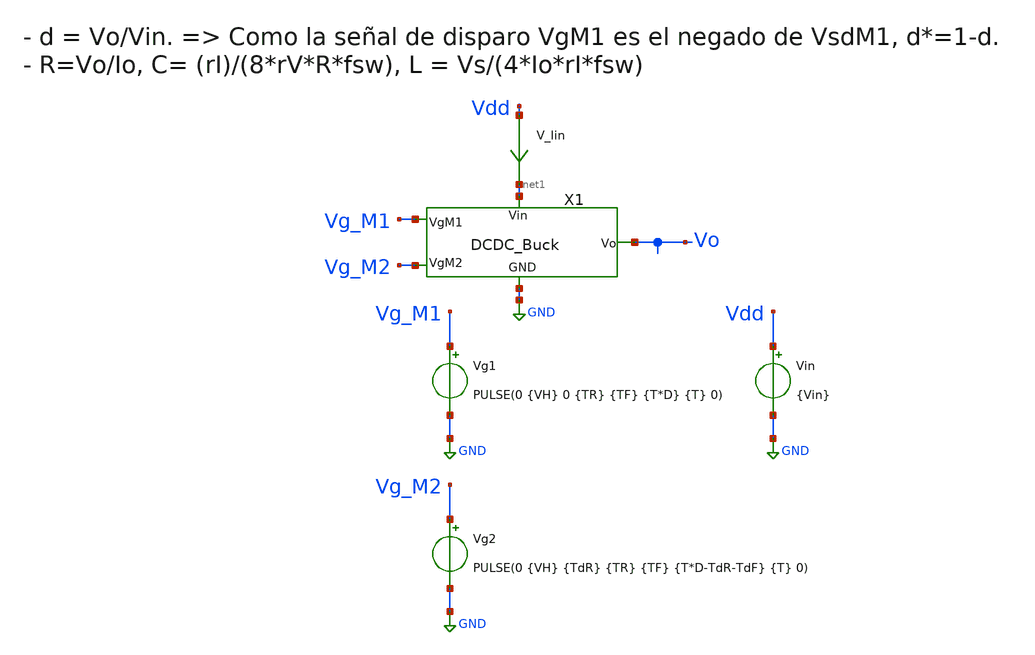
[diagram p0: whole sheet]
** sch_path: xschem/Ayudantias/Ayudantia_1/TB_DCDCBuck.sch
**.subckt TB_DCDCBuck
Vin Vdd GND {Vin}
Vg2 Vg_M2 GND PULSE(0 {VH} {TdR} {TR} {TF} {T*D-TdR-TdF} {T} 0)
Vg1 Vg_M1 GND PULSE(0 {VH} 0 {TR} {TF} {T*D} {T} 0)
V_Iin Vdd net1 0
.save i(v_iin)
X1 Vg_M1 Vg_M2 GND net1 Vo DCDC_Buck
**** begin user architecture code


.param Vin = 3.3
.param VH = 3.3
.param Del = 0

.ic v(Vo) = 0
*.ic i(x1.L1) = 0
*.ic v(Vc) = 0


*.param fsw = 10Meg
*.param fsw = 8.5Meg
.param fsw = 1Meg

.param Vo = 1.8
.param Io = 500m
.param rI = 0.3
.param rV = 0.1
.param T = 1/fsw

.param D = 1-((Vo+0.05)/(Vin-0.03))
.param TR = 0.01*T
.param TF = 0.01*T
.param TdR = 1n
.param TdF = 1n

*Filtro
.param L = Vin/(4*Io*rI*fsw)
.param R = Vo/Io
.param C = rI/(8*rV*R*fsw)

*.option temp = 125
*.option temp = -40
.option temp = 27





.save all
.param tau = 4*L/R
.csparam tau = {tau}
.param SimTime = tau+10*T
.csparam Sim_end = {SimTime}
.csparam Vo = {Vo}
.csparam T = {T}
.csparam L = {L}
.csparam C = {C}
.csparam R = {R}
.csparam fsw = {fsw}

.tran 10n {SimTime} uic

.control
set color0 = white

let strt = 500k
let stp = 10Meg
let step = 500k

compose fsw_sweep start = 500k stop = 10Meg step = 500k

let T_sweep = 1/fsw_sweep
let len = 1+(stp-strt)/step

let eff_sweep = vector(len)
*let fsw_sweep = vector(len)
let Io_sweep = vector(len)
let Vo_sweep = vector(len)
let Po_sweep = vector(len)
let Pin_sweep = vector(len)
let loss_M1_sweep = vector(len)
let loss_M2_sweep = vector(len)

let index = 0

foreach T_val $&T_sweep
	alterparam fsw = $fsw_val
	alterparam T = $T_val
	reset
	save all
	run
	let Io = i(v.x1.V_Io)
	*let Id_M1 = @m.x1.xm1.msky130_fd_pr__pfet_01v8[id]
	let Id_M1 = i(V_Iin)
	*let Id_M2 = @m.x1.xm2.msky130_fd_pr__nfet_01v8[id]
	let Id_M2 = -i(v.x1.V_IM2)
	let gds_M1 = @m.x1.xm1.msky130_fd_pr__pfet_01v8[gds]
	let gds_M2 = @m.x1.xm2.msky130_fd_pr__nfet_01v8[gds]

	let Po = Io*v(Vo)
	let I_in = i(V_Iin)
	let Pin = I_in*v(Vdd)
	let Vsd_M1 = v(Vdd) - v(x1.Vc)
	let Vds_M2 = v(x1.Vc)
	let P_M1 = Vsd_M1*Id_M1
	let P_M2 = -Vds_M2*Id_M2
	let Ron_M1 = Vsd_M1/Id_M1
	let Ron_M2 = Vds_M2/Id_M2
	*let Ron_M1 = 1/gds_M1
	*let Ron_M2 = 1/gds_M2

	let Tmeas_i = {Sim_end} - 5*{T}
	let Tmeas_end = {Sim_end}

	*plot v(Vo)
	*plot Io i(v.x1.V_IL)
	*plot Id_M1 Id_M2
	*plot Po Pin
	*plot P_M1 P_M2
	*plot v(x1.Vc)
	*plot v(Vg_M1) v(Vg_M2)
	*plot Ron_M1 Ron_M2

	meas tran Vo_mean AVG v(Vo) FROM={Tmeas_i} TO={Tmeas_end}
	meas tran Io_mean AVG Io FROM={Tmeas_i} TO={Tmeas_end}
	meas tran Irms_M1 RMS Id_M1 FROM={Tmeas_i} TO={Tmeas_end}
	meas tran Irms_M2 RMS Id_M2 FROM={Tmeas_i} TO={Tmeas_end}
	meas tran Po_mean AVG Po FROM={Tmeas_i} TO={Tmeas_end}
	meas tran Pin_mean AVG Pin FROM={Tmeas_i} TO={Tmeas_end}
	meas tran P_M1_mean AVG P_M1 FROM={Tmeas_i} TO={Tmeas_end}
	meas tran P_M2_mean AVG P_M2 FROM={Tmeas_i} TO={Tmeas_end}

	let eff = 100*Po_mean/Pin_mean
	let loss_M1 = 100*P_M1_mean/Pin_mean
	let loss_M2 = 100*P_M2_mean/Pin_mean
	let cond_loss_M1 = Irms_M1*Irms_M1*40m*100
	let cond_loss_M2 = Irms_M2*Irms_M2*35m*100
	let sumaPot = eff+loss_M1+loss_M2
	print eff loss_M1 loss_M2 cond_loss_M1 cond_loss_M2 sumaPot
	print tau T L C R

	let eff_sweep[index] =  eff
	let Io_sweep[index] = Io_mean
	let Vo_sweep[index] = Vo_mean
	let Po_sweep[index] = Po_mean
	let Pin_sweep[index] = Pin_mean

	let loss_M1_sweep[index] = loss_M1
	let loss_M2_sweep[index] = loss_M2

	let index = index + 1

	*write TB_DCDCBuck.raw
end
*print eff loss_M1_sweep loss_M2_sweep
print eff_sweep loss_M2_sweep loss_M1_sweep
print fsw_sweep Io_sweep Vo_sweep
print Po_sweep Pin_sweep
plot eff_sweep vs fsw_sweep
plot Io_sweep vs fsw_sweep
plot Vo_sweep vs fsw_sweep
plot Pin_sweep Po_sweep vs fsw_sweep
plot loss_M1_sweep loss_M2_sweep vs fsw_sweep
.endc


.end




.lib cornerMOShv.lib mos_tt
.lib cornerMOSlv.lib mos_tt
*.lib cornerMOShv.lib mos_ff
*.lib cornerMOSlv.lib mos_ff
*.lib cornerMOShv.lib mos_ss
*.lib cornerMOSlv.lib mos_ss
*.lib cornerMOShv.lib mos_sf
*.lib cornerMOSlv.lib mos_sf
*.lib cornerMOShv.lib mos_fs
*.lib cornerMOSlv.lib mos_fs

.include /opt/pdks/ihp-sg13g2/libs.ref/sg13g2_stdcell/spice/sg13g2_stdcell.spice
.lib $::SG13G2_MODELS/cornerRES.lib res_typ
.lib $::SG13G2_MODELS/cornerCAP.lib cap_typ
*.lib $::SG13G2_MODELS/diodes.lib



.param temp=27
.param mult_M1 = 3*800
.param w_M1 =10u
.param l_M1 = 0.4u
.param ng_M1 = 1

.param mult_M2 = 800
.param w_M2 =10u
.param l_M2 =0.45u
.param ng_M2 =1








**** end user architecture code
**.ends

* expanding   symbol:  ../Ayudantia_1/DCDC_Buck.sym # of pins=5
** sym_path: xschem/Ayudantias/Ayudantia_1/DCDC_Buck.sym
** sch_path: xschem/Ayudantias/Ayudantia_1/DCDC_Buck.sch
.subckt DCDC_Buck VgM1 VgM2 GND Vin Vo
*.iopin Vin
*.ipin VgM1
*.ipin VgM2
*.iopin Vo
*.iopin GND
L1 net2 net1 {L} m=1
C1 net1 GND {C} m=1
V_Io net1 Vo 0
.save i(v_io)
V_IL Vc net2 0
.save i(v_il)
R1 Vo GND {R} m=1
V_IM2 Vc net3 0
.save i(v_im2)
XM3 Vc VgM1 Vin Vin sg13_hv_pmos w={w_M1} l={l_M1} ng={ng_M1} m={mult_M1} mm_ok=1
XM1 GND VgM2 net3 GND sg13_hv_nmos w={w_M2} l={l_M2} ng={ng_M2} m={mult_M2} mm_ok=1
.ends

.GLOBAL GND
.end
